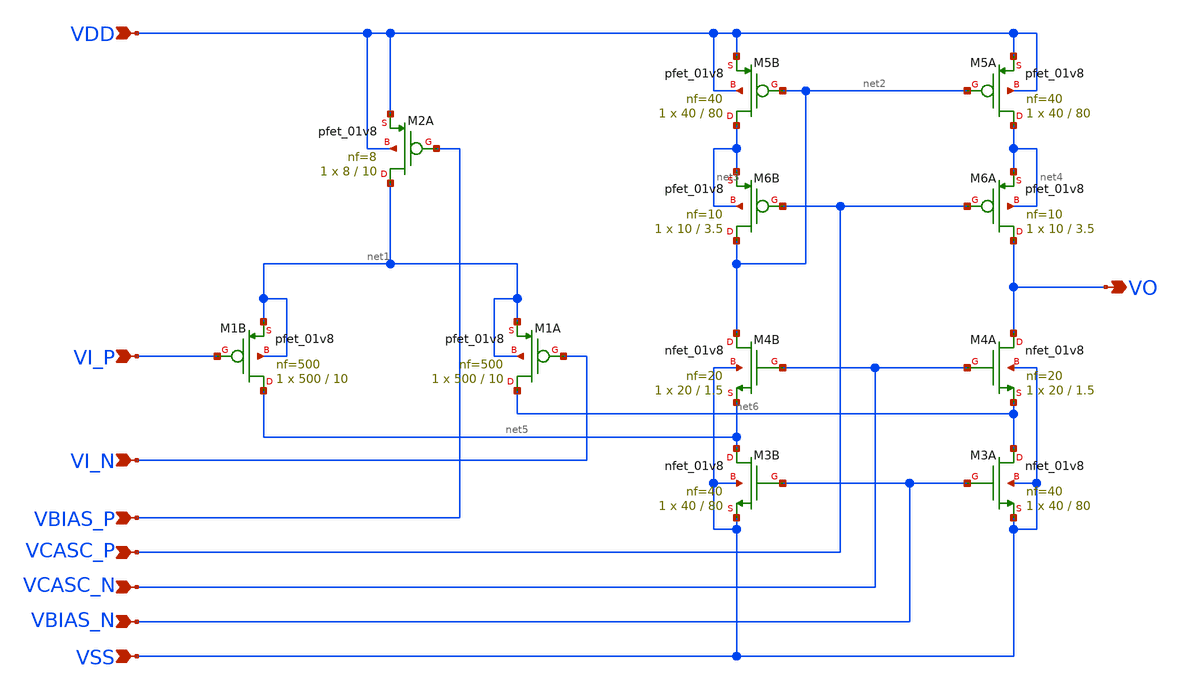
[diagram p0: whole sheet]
** sch_path: circuit-level/xschem/aux-amp/amp_gm_boost_2.sch
**.subckt amp_gm_boost_2 VDD VI_N VI_P VBIAS_P VBIAS_N VCASC_N VCASC_P VO VSS
*.ipin VDD
*.ipin VI_N
*.ipin VI_P
*.ipin VBIAS_P
*.ipin VBIAS_N
*.ipin VCASC_N
*.ipin VCASC_P
*.opin VO
*.ipin VSS
XM2A net1 VBIAS_P VDD VDD sky130_fd_pr__pfet_01v8 L=10 W=8 nf=8 ad='int((nf+1)/2) * W/nf * 0.29' as='int((nf+2)/2) * W/nf * 0.29'
+ pd='2*int((nf+1)/2) * (W/nf + 0.29)' ps='2*int((nf+2)/2) * (W/nf + 0.29)' nrd='0.29 / W' nrs='0.29 / W'
+ sa=0 sb=0 sd=0 mult=1 m=1
XM1B net5 VI_P net1 net1 sky130_fd_pr__pfet_01v8 L=10 W=500 nf=500 ad='int((nf+1)/2) * W/nf * 0.29' as='int((nf+2)/2) * W/nf * 0.29'
+ pd='2*int((nf+1)/2) * (W/nf + 0.29)' ps='2*int((nf+2)/2) * (W/nf + 0.29)' nrd='0.29 / W' nrs='0.29 / W'
+ sa=0 sb=0 sd=0 mult=1 m=1
XM1A net6 VI_N net1 net1 sky130_fd_pr__pfet_01v8 L=10 W=500 nf=500 ad='int((nf+1)/2) * W/nf * 0.29' as='int((nf+2)/2) * W/nf * 0.29'
+ pd='2*int((nf+1)/2) * (W/nf + 0.29)' ps='2*int((nf+2)/2) * (W/nf + 0.29)' nrd='0.29 / W' nrs='0.29 / W'
+ sa=0 sb=0 sd=0 mult=1 m=1
XM4B net2 VCASC_N net5 VSS sky130_fd_pr__nfet_01v8 L=1.5 W=20 nf=20 ad='int((nf+1)/2) * W/nf * 0.29'
+ as='int((nf+2)/2) * W/nf * 0.29' pd='2*int((nf+1)/2) * (W/nf + 0.29)' ps='2*int((nf+2)/2) * (W/nf + 0.29)'
+ nrd='0.29 / W' nrs='0.29 / W' sa=0 sb=0 sd=0 mult=1 m=1
XM4A VO VCASC_N net6 VSS sky130_fd_pr__nfet_01v8 L=1.5 W=20 nf=20 ad='int((nf+1)/2) * W/nf * 0.29' as='int((nf+2)/2) * W/nf * 0.29'
+ pd='2*int((nf+1)/2) * (W/nf + 0.29)' ps='2*int((nf+2)/2) * (W/nf + 0.29)' nrd='0.29 / W' nrs='0.29 / W'
+ sa=0 sb=0 sd=0 mult=1 m=1
XM3B net5 VBIAS_N VSS VSS sky130_fd_pr__nfet_01v8 L=80 W=40 nf=40 ad='int((nf+1)/2) * W/nf * 0.29' as='int((nf+2)/2) * W/nf * 0.29'
+ pd='2*int((nf+1)/2) * (W/nf + 0.29)' ps='2*int((nf+2)/2) * (W/nf + 0.29)' nrd='0.29 / W' nrs='0.29 / W'
+ sa=0 sb=0 sd=0 mult=1 m=1
XM3A net6 VBIAS_N VSS VSS sky130_fd_pr__nfet_01v8 L=80 W=40 nf=40 ad='int((nf+1)/2) * W/nf * 0.29' as='int((nf+2)/2) * W/nf * 0.29'
+ pd='2*int((nf+1)/2) * (W/nf + 0.29)' ps='2*int((nf+2)/2) * (W/nf + 0.29)' nrd='0.29 / W' nrs='0.29 / W'
+ sa=0 sb=0 sd=0 mult=1 m=1
XM5B net3 net2 VDD VDD sky130_fd_pr__pfet_01v8 L=80 W=40 nf=40 ad='int((nf+1)/2) * W/nf * 0.29' as='int((nf+2)/2) * W/nf * 0.29'
+ pd='2*int((nf+1)/2) * (W/nf + 0.29)' ps='2*int((nf+2)/2) * (W/nf + 0.29)' nrd='0.29 / W' nrs='0.29 / W'
+ sa=0 sb=0 sd=0 mult=1 m=1
XM5A net4 net2 VDD VDD sky130_fd_pr__pfet_01v8 L=80 W=40 nf=40 ad='int((nf+1)/2) * W/nf * 0.29' as='int((nf+2)/2) * W/nf * 0.29'
+ pd='2*int((nf+1)/2) * (W/nf + 0.29)' ps='2*int((nf+2)/2) * (W/nf + 0.29)' nrd='0.29 / W' nrs='0.29 / W'
+ sa=0 sb=0 sd=0 mult=1 m=1
XM6B net2 VCASC_P net3 net3 sky130_fd_pr__pfet_01v8 L=3.5 W=10 nf=10 ad='int((nf+1)/2) * W/nf * 0.29'
+ as='int((nf+2)/2) * W/nf * 0.29' pd='2*int((nf+1)/2) * (W/nf + 0.29)' ps='2*int((nf+2)/2) * (W/nf + 0.29)'
+ nrd='0.29 / W' nrs='0.29 / W' sa=0 sb=0 sd=0 mult=1 m=1
XM6A VO VCASC_P net4 net4 sky130_fd_pr__pfet_01v8 L=3.5 W=10 nf=10 ad='int((nf+1)/2) * W/nf * 0.29' as='int((nf+2)/2) * W/nf * 0.29'
+ pd='2*int((nf+1)/2) * (W/nf + 0.29)' ps='2*int((nf+2)/2) * (W/nf + 0.29)' nrd='0.29 / W' nrs='0.29 / W'
+ sa=0 sb=0 sd=0 mult=1 m=1
**.ends
.end
